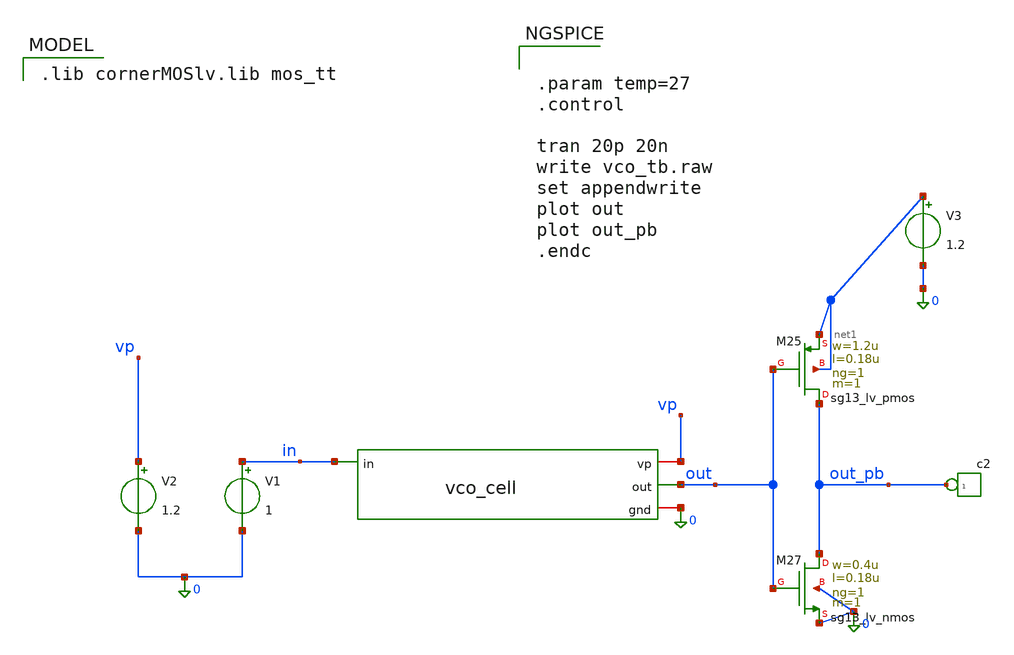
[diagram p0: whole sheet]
** sch_path: vco/vco_tb/vco_tb.sch
**.subckt vco_tb
x1 vp out in 0 vco_cell
V1 in 0 1
V2 vp 0 1.2
*connector(1,1) ?1 out_pb
XM25 out_pb out net1 net1 sg13_lv_pmos w=1.2u l=0.18u ng=1 m=1 mm_ok=1
XM27 out_pb out 0 0 sg13_lv_nmos w=0.4u l=0.18u ng=1 m=1 mm_ok=1
V3 net1 0 1.2
**** begin user architecture code


.param temp=27
.control

tran 20p 20n
write vco_tb.raw
set appendwrite
plot out
plot out_pb
.endc


 .lib cornerMOSlv.lib mos_tt

**** end user architecture code
**.ends

* expanding   symbol:  /foss/designs/CHIP-PLL/vco/vco_cell.sym # of pins=4
** sym_path: schematics/vco/vco_cell/vco_cell.sym
** sch_path: schematics/vco/vco_cell/vco_cell.sch
.subckt vco_cell vp out in gnd
*.ipin in
*.iopin gnd
*.iopin vp
*.opin out
XM1 chwcto in gnd gnd sg13_lv_nmos w=0.405u l=0.420u ng=1 m=1 mm_ok=1
XM2 chwcto chwcto vp vp sg13_lv_pmos w=1.21u l=0.18u ng=1 m=1 mm_ok=1
XM3 1up chwcto vp vp sg13_lv_pmos w=1.21u l=0.18u ng=1 m=1 mm_ok=1
XM4 2up chwcto vp vp sg13_lv_pmos w=1.21u l=0.18u ng=1 m=1 mm_ok=1
XM5 3up chwcto vp vp sg13_lv_pmos w=1.21u l=0.18u ng=1 m=1 mm_ok=1
XM6 4up chwcto vp vp sg13_lv_pmos w=1.21u l=0.18u ng=1 m=1 mm_ok=1
XM7 5up chwcto vp vp sg13_lv_pmos w=1.21u l=0.18u ng=1 m=1 mm_ok=1
XM8 1-2 out 1up 1up sg13_lv_pmos w=1.2u l=0.18u ng=1 m=1 mm_ok=1
XM9 2-3 1-2 2up 2up sg13_lv_pmos w=1.2u l=0.18u ng=1 m=1 mm_ok=1
XM10 3-4 2-3 3up 3up sg13_lv_pmos w=1.2u l=0.18u ng=1 m=1 mm_ok=1
XM11 4-5 3-4 4up 4up sg13_lv_pmos w=1.2u l=0.18u ng=1 m=1 mm_ok=1
XM12 out 4-5 5up 5up sg13_lv_pmos w=1.2u l=0.18u ng=1 m=1 mm_ok=1
XM13 1-2 out 1dn 1dn sg13_lv_nmos w=0.4u l=0.18u ng=1 m=1 mm_ok=1
XM14 2-3 1-2 2dn 2dn sg13_lv_nmos w=0.4u l=0.18u ng=1 m=1 mm_ok=1
XM15 3-4 2-3 3dn 3dn sg13_lv_nmos w=0.4u l=0.18u ng=1 m=1 mm_ok=1
XM16 4-5 3-4 4dn 4dn sg13_lv_nmos w=0.4u l=0.18u ng=1 m=1 mm_ok=1
XM17 out 4-5 5dn 5dn sg13_lv_nmos w=0.4u l=0.18u ng=1 m=1 mm_ok=1
XM18 1dn in gnd gnd sg13_lv_nmos w=0.405u l=0.420u ng=1 m=1 mm_ok=1
XM19 2dn in gnd gnd sg13_lv_nmos w=0.405u l=0.420u ng=1 m=1 mm_ok=1
XM20 3dn in gnd gnd sg13_lv_nmos w=0.405u l=0.420u ng=1 m=1 mm_ok=1
XM21 4dn in gnd gnd sg13_lv_nmos w=0.405u l=0.420u ng=1 m=1 mm_ok=1
XM22 5dn in gnd gnd sg13_lv_nmos w=0.405u l=0.420u ng=1 m=1 mm_ok=1
.ends

.end
